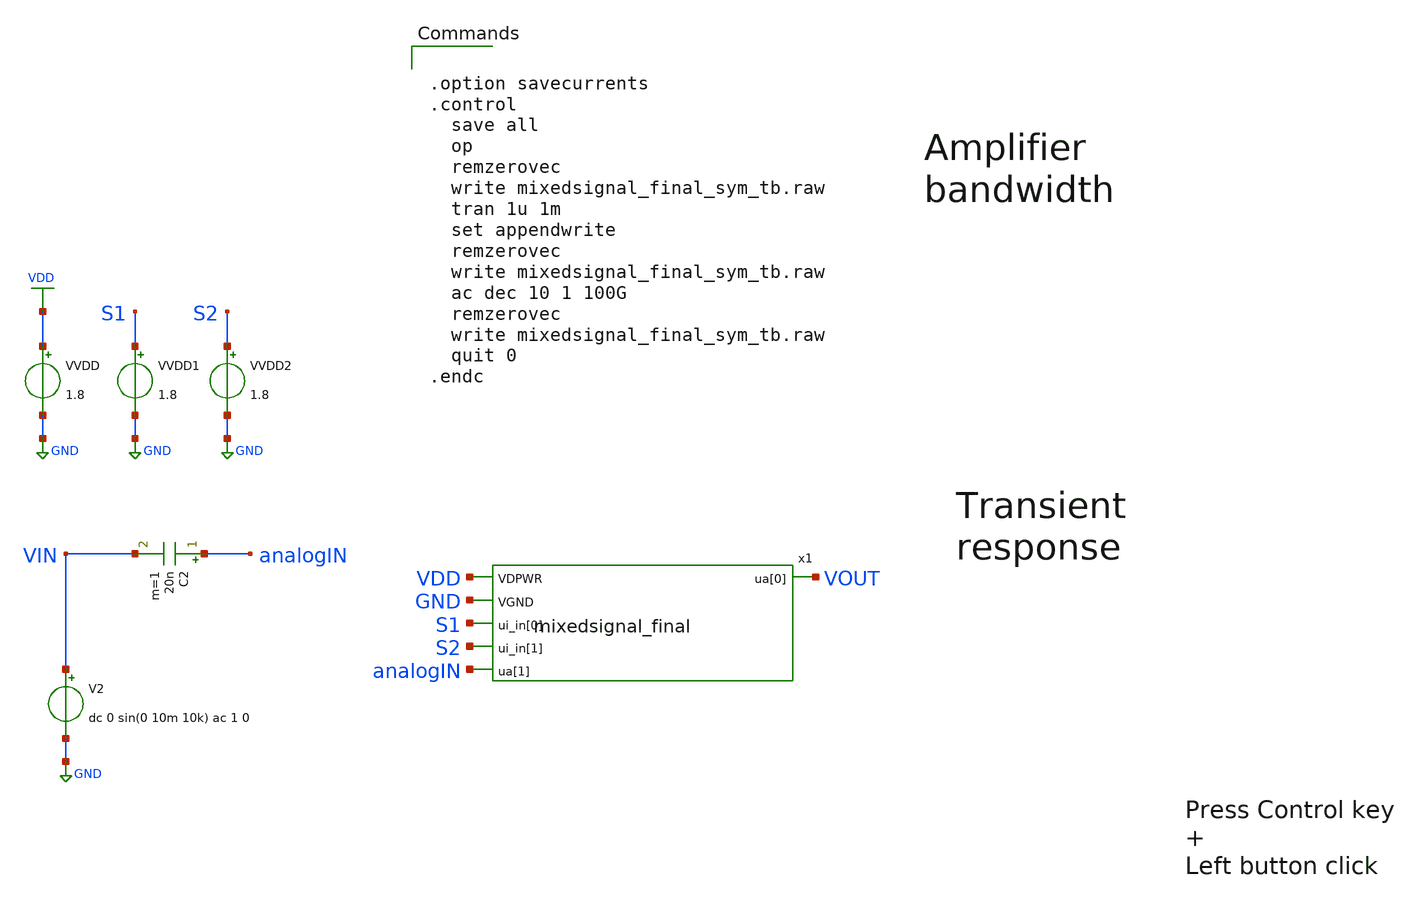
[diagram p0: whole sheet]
** sch_path: xschem/mixedsignal_final_sym_tb.sch
**.subckt mixedsignal_final_sym_tb
x1 VDD GND S1 S2 analogIN VOUT mixedsignal_final
VVDD VDD GND 1.8
C2 analogIN VIN 20n m=1
V2 VIN GND dc 0 sin(0 10m 10k) ac 1 0
VVDD2 S2 GND 1.8
VVDD1 S1 GND 1.8
**** begin user architecture code

** opencircuitdesign pdks install
.lib $::SKYWATER_MODELS/sky130.lib.spice tt




.option savecurrents
.control
  save all
  op
  remzerovec
  write mixedsignal_final_sym_tb.raw
  tran 1u 1m
  set appendwrite
  remzerovec
  write mixedsignal_final_sym_tb.raw
  ac dec 10 1 100G
  remzerovec
  write mixedsignal_final_sym_tb.raw
  quit 0
.endc


**** end user architecture code
**.ends

* expanding   symbol:  mixedsignal_final.sym # of pins=6
** sym_path: xschem/mixedsignal_final.sym
** sch_path: xschem/mixedsignal_final.sch
.subckt mixedsignal_final VDPWR VGND ui_in[0] ui_in[1] ua[1] ua[0]
*.opin ua[0]
*.ipin ua[1]
*.ipin ui_in[0]
*.ipin ui_in[1]
*.ipin VDPWR
*.ipin VGND
x1 ui_in[0] ui_in[1] VDPWR VGND net4 net1 mux_in net2 net3 4-to-1_analog_MUX
* noconn ua[0]
* noconn #net4
XR3 ua[0] net1 VGND sky130_fd_pr__res_xhigh_po_5p73 L=8.6 mult=1 m=1
XR2 ua[0] net2 VGND sky130_fd_pr__res_xhigh_po_5p73 L=86 mult=1 m=1
XR4 ua[0] mux_in VGND sky130_fd_pr__res_xhigh_po_5p73 L=860 mult=1 m=1
XR1 mux_in ua[1] VGND sky130_fd_pr__res_xhigh_po_5p73 L=8.6 mult=1 m=1
XR5 ua[0] net3 VGND sky130_fd_pr__res_xhigh_po_5p73 L=287 mult=1 m=1
XM1 ua[0] mux_in VDPWR VDPWR sky130_fd_pr__pfet_01v8 L=0.5 W=4 nf=5 ad='int((nf+1)/2) * W/nf * 0.29'
+ as='int((nf+2)/2) * W/nf * 0.29' pd='2*int((nf+1)/2) * (W/nf + 0.29)' ps='2*int((nf+2)/2) * (W/nf + 0.29)'
+ nrd='0.29 / W' nrs='0.29 / W' sa=0 sb=0 sd=0 mult=1 m=1
XM10 ua[0] mux_in VGND VGND sky130_fd_pr__nfet_01v8 L=0.5 W=4 nf=5 ad='int((nf+1)/2) * W/nf * 0.29' as='int((nf+2)/2) * W/nf * 0.29'
+ pd='2*int((nf+1)/2) * (W/nf + 0.29)' ps='2*int((nf+2)/2) * (W/nf + 0.29)' nrd='0.29 / W' nrs='0.29 / W'
+ sa=0 sb=0 sd=0 mult=1 m=1
.ends


* expanding   symbol:  4-to-1_analog_MUX.sym # of pins=9
** sym_path: xschem/4-to-1_analog_MUX.sym
** sch_path: xschem/4-to-1_analog_MUX.sch
.subckt 4-to-1_analog_MUX S1 S2 VDD GND I1 I2 OUT I3 I4
*.ipin I1
*.ipin I2
*.ipin I3
*.ipin I4
*.opin OUT
*.ipin S1
*.ipin S2
*.ipin VDD
*.ipin GND
x1 S1 S1bar GND VDD Inverter
x2 S2 S2bar GND VDD Inverter
XM9 net1 S2 OUT VDD sky130_fd_pr__pfet_01v8 L=0.5 W=1 nf=1 ad='int((nf+1)/2) * W/nf * 0.29' as='int((nf+2)/2) * W/nf * 0.29'
+ pd='2*int((nf+1)/2) * (W/nf + 0.29)' ps='2*int((nf+2)/2) * (W/nf + 0.29)' nrd='0.29 / W' nrs='0.29 / W'
+ sa=0 sb=0 sd=0 mult=1 m=1
XM1 I1 S1 net1 VDD sky130_fd_pr__pfet_01v8 L=0.5 W=1 nf=1 ad='int((nf+1)/2) * W/nf * 0.29' as='int((nf+2)/2) * W/nf * 0.29'
+ pd='2*int((nf+1)/2) * (W/nf + 0.29)' ps='2*int((nf+2)/2) * (W/nf + 0.29)' nrd='0.29 / W' nrs='0.29 / W'
+ sa=0 sb=0 sd=0 mult=1 m=1
XM2 I3 S1bar net1 VDD sky130_fd_pr__pfet_01v8 L=0.5 W=1 nf=1 ad='int((nf+1)/2) * W/nf * 0.29' as='int((nf+2)/2) * W/nf * 0.29'
+ pd='2*int((nf+1)/2) * (W/nf + 0.29)' ps='2*int((nf+2)/2) * (W/nf + 0.29)' nrd='0.29 / W' nrs='0.29 / W'
+ sa=0 sb=0 sd=0 mult=1 m=1
XM5 I2 S1 net2 VDD sky130_fd_pr__pfet_01v8 L=0.5 W=1 nf=1 ad='int((nf+1)/2) * W/nf * 0.29' as='int((nf+2)/2) * W/nf * 0.29'
+ pd='2*int((nf+1)/2) * (W/nf + 0.29)' ps='2*int((nf+2)/2) * (W/nf + 0.29)' nrd='0.29 / W' nrs='0.29 / W'
+ sa=0 sb=0 sd=0 mult=1 m=1
XM7 I4 S1bar net2 VDD sky130_fd_pr__pfet_01v8 L=0.5 W=1 nf=1 ad='int((nf+1)/2) * W/nf * 0.29' as='int((nf+2)/2) * W/nf * 0.29'
+ pd='2*int((nf+1)/2) * (W/nf + 0.29)' ps='2*int((nf+2)/2) * (W/nf + 0.29)' nrd='0.29 / W' nrs='0.29 / W'
+ sa=0 sb=0 sd=0 mult=1 m=1
XM11 net2 S2bar OUT VDD sky130_fd_pr__pfet_01v8 L=0.5 W=1 nf=1 ad='int((nf+1)/2) * W/nf * 0.29' as='int((nf+2)/2) * W/nf * 0.29'
+ pd='2*int((nf+1)/2) * (W/nf + 0.29)' ps='2*int((nf+2)/2) * (W/nf + 0.29)' nrd='0.29 / W' nrs='0.29 / W'
+ sa=0 sb=0 sd=0 mult=1 m=1
XM3 I1 S1bar net1 GND sky130_fd_pr__nfet_01v8 L=1 W=1 nf=1 ad='int((nf+1)/2) * W/nf * 0.29' as='int((nf+2)/2) * W/nf * 0.29'
+ pd='2*int((nf+1)/2) * (W/nf + 0.29)' ps='2*int((nf+2)/2) * (W/nf + 0.29)' nrd='0.29 / W' nrs='0.29 / W'
+ sa=0 sb=0 sd=0 mult=1 m=1
XM4 I3 S1 net1 GND sky130_fd_pr__nfet_01v8 L=1 W=1 nf=1 ad='int((nf+1)/2) * W/nf * 0.29' as='int((nf+2)/2) * W/nf * 0.29'
+ pd='2*int((nf+1)/2) * (W/nf + 0.29)' ps='2*int((nf+2)/2) * (W/nf + 0.29)' nrd='0.29 / W' nrs='0.29 / W'
+ sa=0 sb=0 sd=0 mult=1 m=1
XM10 net1 S2bar OUT GND sky130_fd_pr__nfet_01v8 L=1 W=1 nf=1 ad='int((nf+1)/2) * W/nf * 0.29' as='int((nf+2)/2) * W/nf * 0.29'
+ pd='2*int((nf+1)/2) * (W/nf + 0.29)' ps='2*int((nf+2)/2) * (W/nf + 0.29)' nrd='0.29 / W' nrs='0.29 / W'
+ sa=0 sb=0 sd=0 mult=1 m=1
XM6 I2 S1bar net2 GND sky130_fd_pr__nfet_01v8 L=1 W=1 nf=1 ad='int((nf+1)/2) * W/nf * 0.29' as='int((nf+2)/2) * W/nf * 0.29'
+ pd='2*int((nf+1)/2) * (W/nf + 0.29)' ps='2*int((nf+2)/2) * (W/nf + 0.29)' nrd='0.29 / W' nrs='0.29 / W'
+ sa=0 sb=0 sd=0 mult=1 m=1
XM8 I4 S1 net2 GND sky130_fd_pr__nfet_01v8 L=1 W=1 nf=1 ad='int((nf+1)/2) * W/nf * 0.29' as='int((nf+2)/2) * W/nf * 0.29'
+ pd='2*int((nf+1)/2) * (W/nf + 0.29)' ps='2*int((nf+2)/2) * (W/nf + 0.29)' nrd='0.29 / W' nrs='0.29 / W'
+ sa=0 sb=0 sd=0 mult=1 m=1
XM12 net2 S2 OUT GND sky130_fd_pr__nfet_01v8 L=1 W=1 nf=1 ad='int((nf+1)/2) * W/nf * 0.29' as='int((nf+2)/2) * W/nf * 0.29'
+ pd='2*int((nf+1)/2) * (W/nf + 0.29)' ps='2*int((nf+2)/2) * (W/nf + 0.29)' nrd='0.29 / W' nrs='0.29 / W'
+ sa=0 sb=0 sd=0 mult=1 m=1
.ends


* expanding   symbol:  Inverter.sym # of pins=4
** sym_path: xschem/Inverter.sym
** sch_path: xschem/Inverter.sch
.subckt Inverter Vin Vout GND VDD
*.opin Vout
*.ipin Vin
*.ipin VDD
*.ipin GND
XM1 Vout Vin VDD VDD sky130_fd_pr__pfet_01v8 L=0.5 W=1 nf=1 ad='int((nf+1)/2) * W/nf * 0.29' as='int((nf+2)/2) * W/nf * 0.29'
+ pd='2*int((nf+1)/2) * (W/nf + 0.29)' ps='2*int((nf+2)/2) * (W/nf + 0.29)' nrd='0.29 / W' nrs='0.29 / W'
+ sa=0 sb=0 sd=0 mult=1 m=1
XM2 Vout Vin GND GND sky130_fd_pr__nfet_01v8 L=1 W=1 nf=1 ad='int((nf+1)/2) * W/nf * 0.29' as='int((nf+2)/2) * W/nf * 0.29'
+ pd='2*int((nf+1)/2) * (W/nf + 0.29)' ps='2*int((nf+2)/2) * (W/nf + 0.29)' nrd='0.29 / W' nrs='0.29 / W'
+ sa=0 sb=0 sd=0 mult=1 m=1
.ends

.GLOBAL GND
.GLOBAL VDD
.end
